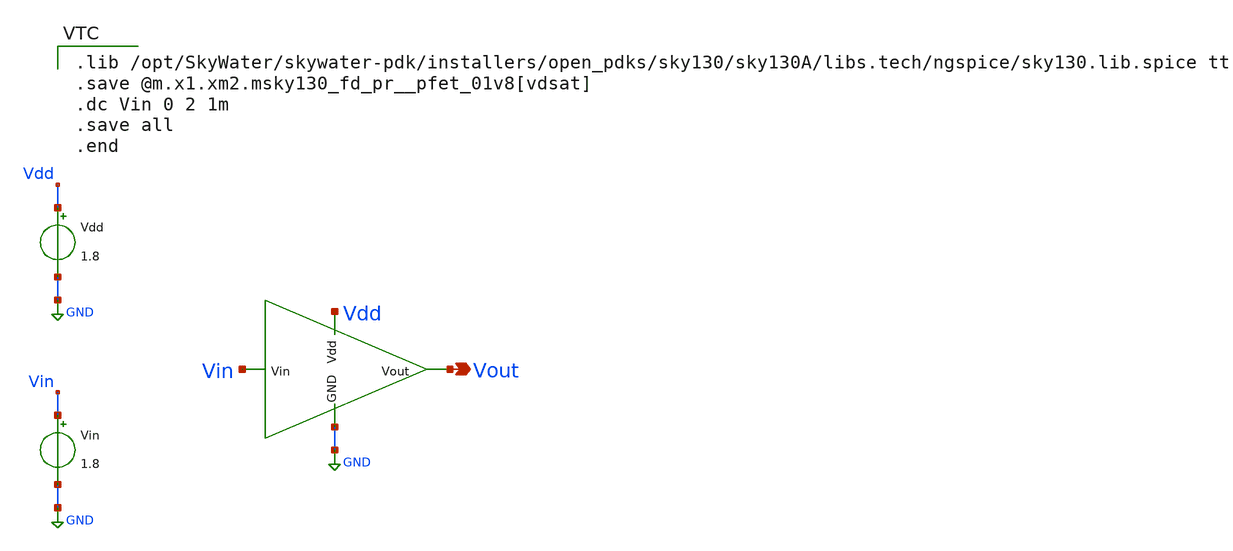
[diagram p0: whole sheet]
** sch_path: 1/xschem/inverter_test.sch
**.subckt inverter_test Vout
*.opin Vout
x1 Vdd Vout Vin GND inverter
Vdd Vdd GND 1.8
.save i(vdd)
Vin Vin GND 1.8
.save i(vin)
**** begin user architecture code

.lib /opt/SkyWater/skywater-pdk/installers/open_pdks/sky130/sky130A/libs.tech/ngspice/sky130.lib.spice tt
.save @m.x1.xm2.msky130_fd_pr__pfet_01v8[vdsat]
.dc Vin 0 2 1m
.save all
.end

**** end user architecture code
**.ends
.GLOBAL GND
.end
